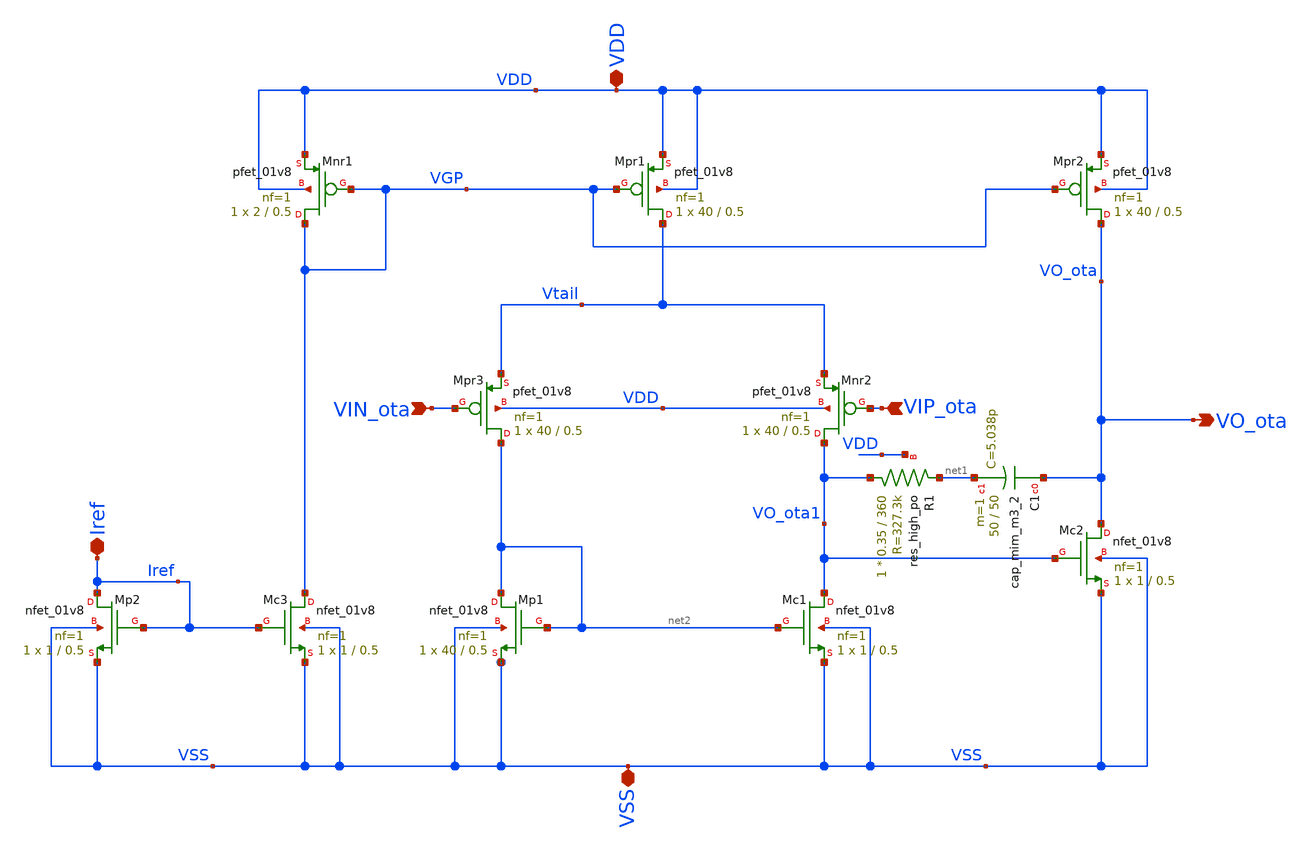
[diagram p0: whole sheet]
** sch_path: untitled-1.sch
**.subckt untitled-1 VIN_ota VO_ota Iref VSS VDD VIP_ota
*.ipin VIN_ota
*.opin VO_ota
*.iopin Iref
*.iopin VSS
*.iopin VDD
*.ipin VIP_ota
XR1 VO_ota1 net1 VDD sky130_fd_pr__res_high_po W=0.35 L=360 mult=1 m=1
XC1 VO_ota net1 sky130_fd_pr__cap_mim_m3_2 W=50 L=50 MF=1 m=1
XMnr1 VGP VGP VDD VDD sky130_fd_pr__pfet_01v8 L=0.5 W=2 nf=1 ad='int((1 + 1)/2) * 2 / 1 * 0.29' as='int((1 + 2)/2) * 2 / 1 * 0.29'
+ pd='2*int((1 + 1)/2) * (2 / 1 + 0.29)' ps='2*int((1 + 2)/2) * (2 / 1 + 0.29)' nrd='0.29 / 2 ' nrs='0.29 / 2 '
+ sa=0 sb=0 sd=0 mult=1 m=1
XMc1 VO_ota1 net2 VSS VSS sky130_fd_pr__nfet_01v8 L=0.5 W=1 nf=1 ad='int((1 + 1)/2) * 1 / 1 * 0.29' as='int((1 + 2)/2) * 1 / 1 * 0.29'
+ pd='2*int((1 + 1)/2) * (1 / 1 + 0.29)' ps='2*int((1 + 2)/2) * (1 / 1 + 0.29)' nrd='0.29 / 1 ' nrs='0.29 / 1 '
+ sa=0 sb=0 sd=0 mult=1 m=1
XMp1 net2 net2 VSS VSS sky130_fd_pr__nfet_01v8 L=0.5 W=40 nf=1 ad='int((1 + 1)/2) * 40 / 1 * 0.29' as='int((1 + 2)/2) * 40 / 1 * 0.29'
+ pd='2*int((1 + 1)/2) * (40 / 1 + 0.29)' ps='2*int((1 + 2)/2) * (40 / 1 + 0.29)' nrd='0.29 / 40 ' nrs='0.29 / 40 '
+ sa=0 sb=0 sd=0 mult=1 m=1
XMpr1 Vtail VGP VDD VDD sky130_fd_pr__pfet_01v8 L=0.5 W=40 nf=1 ad='int((1 + 1)/2) * 40 / 1 * 0.29' as='int((1 + 2)/2) * 40 / 1 * 0.29'
+ pd='2*int((1 + 1)/2) * (40 / 1 + 0.29)' ps='2*int((1 + 2)/2) * (40 / 1 + 0.29)' nrd='0.29 / 40 ' nrs='0.29 / 40 '
+ sa=0 sb=0 sd=0 mult=1 m=1
XMpr2 VO_ota VGP VDD VDD sky130_fd_pr__pfet_01v8 L=0.5 W=40 nf=1 ad='int((1 + 1)/2) * 40 / 1 * 0.29'
+ as='int((1 + 2)/2) * 40 / 1 * 0.29' pd='2*int((1 + 1)/2) * (40 / 1 + 0.29)' ps='2*int((1 + 2)/2) * (40 / 1 + 0.29)'
+ nrd='0.29 / 40 ' nrs='0.29 / 40 ' sa=0 sb=0 sd=0 mult=1 m=1
XMpr3 net2 VIN_ota Vtail VDD sky130_fd_pr__pfet_01v8 L=0.5 W=40 nf=1 ad='int((1 + 1)/2) * 40 / 1 * 0.29'
+ as='int((1 + 2)/2) * 40 / 1 * 0.29' pd='2*int((1 + 1)/2) * (40 / 1 + 0.29)' ps='2*int((1 + 2)/2) * (40 / 1 + 0.29)'
+ nrd='0.29 / 40 ' nrs='0.29 / 40 ' sa=0 sb=0 sd=0 mult=1 m=1
XMnr2 VO_ota1 VIP_ota Vtail VDD sky130_fd_pr__pfet_01v8 L=0.5 W=40 nf=1 ad='int((1 + 1)/2) * 40 / 1 * 0.29'
+ as='int((1 + 2)/2) * 40 / 1 * 0.29' pd='2*int((1 + 1)/2) * (40 / 1 + 0.29)' ps='2*int((1 + 2)/2) * (40 / 1 + 0.29)'
+ nrd='0.29 / 40 ' nrs='0.29 / 40 ' sa=0 sb=0 sd=0 mult=1 m=1
XMc2 VO_ota VO_ota1 VSS VSS sky130_fd_pr__nfet_01v8 L=0.5 W=1 nf=1 ad='int((1 + 1)/2) * 1 / 1 * 0.29'
+ as='int((1 + 2)/2) * 1 / 1 * 0.29' pd='2*int((1 + 1)/2) * (1 / 1 + 0.29)' ps='2*int((1 + 2)/2) * (1 / 1 + 0.29)'
+ nrd='0.29 / 1 ' nrs='0.29 / 1 ' sa=0 sb=0 sd=0 mult=1 m=1
XMc3 VGP Iref VSS VSS sky130_fd_pr__nfet_01v8 L=0.5 W=1 nf=1 ad='int((1 + 1)/2) * 1 / 1 * 0.29' as='int((1 + 2)/2) * 1 / 1 * 0.29'
+ pd='2*int((1 + 1)/2) * (1 / 1 + 0.29)' ps='2*int((1 + 2)/2) * (1 / 1 + 0.29)' nrd='0.29 / 1 ' nrs='0.29 / 1 '
+ sa=0 sb=0 sd=0 mult=1 m=1
XMp2 Iref Iref VSS VSS sky130_fd_pr__nfet_01v8 L=0.5 W=1 nf=1 ad='int((1 + 1)/2) * 1 / 1 * 0.29' as='int((1 + 2)/2) * 1 / 1 * 0.29'
+ pd='2*int((1 + 1)/2) * (1 / 1 + 0.29)' ps='2*int((1 + 2)/2) * (1 / 1 + 0.29)' nrd='0.29 / 1 ' nrs='0.29 / 1 '
+ sa=0 sb=0 sd=0 mult=1 m=1
**.ends
.end
